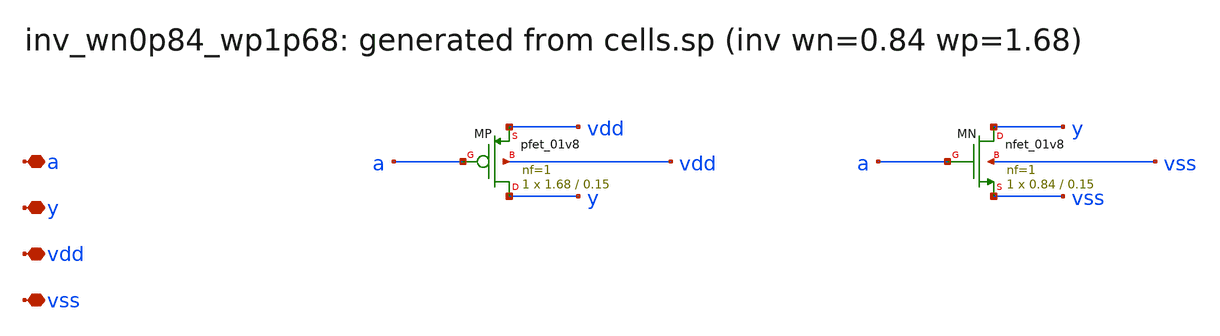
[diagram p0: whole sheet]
** sch_path: sram/xschem/inv_wn0p84_wp1p68.sch
**.subckt inv_wn0p84_wp1p68 a y vdd vss
*.iopin a
*.iopin y
*.iopin vdd
*.iopin vss
XMP y a vdd vdd sky130_fd_pr__pfet_01v8 L=0.15 W=1.68 nf=1 ad='int((nf+1)/2) * W/nf * 0.29' as='int((nf+2)/2) * W/nf * 0.29'
+ pd='2*int((nf+1)/2) * (W/nf + 0.29)' ps='2*int((nf+2)/2) * (W/nf + 0.29)' nrd='0.29 / W' nrs='0.29 / W'
+ sa=0 sb=0 sd=0 mult=1 m=1
XMN y a vss vss sky130_fd_pr__nfet_01v8 L=0.15 W=0.84 nf=1 ad='int((1 + 1)/2) * 0.84 / 1 * 0.29' as='int((1 + 2)/2) * 0.84 / 1 * 0.29'
+ pd='2*int((1 + 1)/2) * (0.84 / 1 + 0.29)' ps='2*int((1 + 2)/2) * (0.84 / 1 + 0.29)' nrd='0.29 / 0.84 '
+ nrs='0.29 / 0.84 ' sa=0 sb=0 sd=0 mult=1 m=1
**.ends
.end
